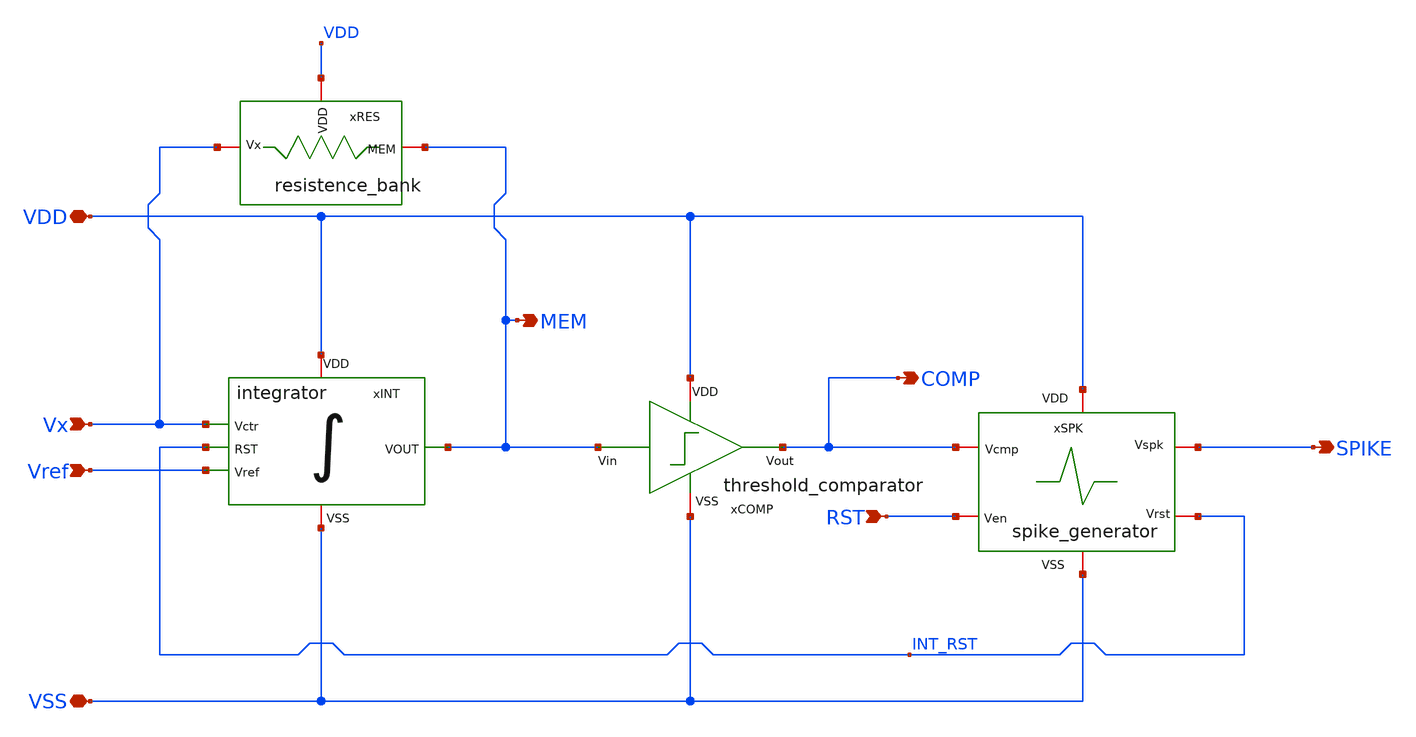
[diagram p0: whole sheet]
** sch_path: OSC9996-main/schematic/xschem/LIF_neuron.sch
**.subckt LIF_neuron VDD VSS MEM Vx Vref SPIKE RST COMP
*.iopin VDD
*.iopin VSS
*.opin MEM
*.ipin Vx
*.ipin Vref
*.opin SPIKE
*.ipin RST
*.opin COMP
xINT Vref VSS VDD INT_RST Vx MEM integrator
xSPK VDD COMP SPIKE INT_RST RST VSS spike_generator
xRES VDD MEM Vx resistence_bank
xCOMP VDD MEM COMP VSS threshold_comparator
**.ends
.end
